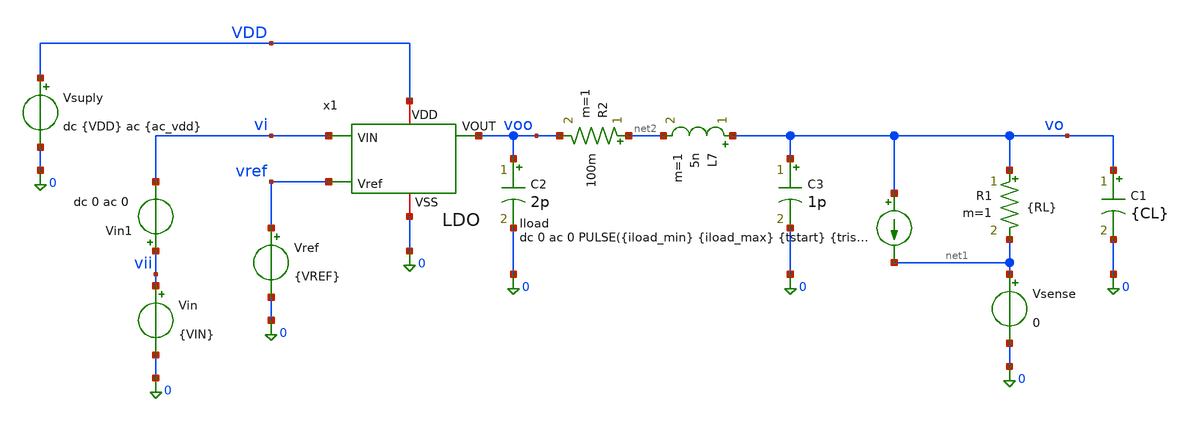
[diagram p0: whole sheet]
** sch_path: xschem/LDO_Top/ldo_tb_pex_montecarlo.sch
**.subckt ldo_tb_pex_montecarlo
Vsuply VDD 0 dc {VDD} ac {ac_vdd}
Vref vref 0 {VREF}
Vin vii 0 {VIN}
R1 vo net1 {RL} m=1
C1 vo 0 {CL} m=1
Iload vo net1 dc 0 ac 0 PULSE({iload_min} {iload_max} {tstart} {trise} {tfall} {twidth} {tperiod})
Vsense net1 0 0
Vin1 vii vi dc 0 ac 0
x1 vi voo VDD vref 0 LDO
C2 voo 0 2p m=1
R2 net2 voo 100m m=1
L7 vo net2 5n m=1
C3 vo 0 1p m=1
**** begin user architecture code


* ==============================================================================
* ENCABEZADO DEL ARCHIVO:
* Script de simulación Monte Carlo Post-Layout (PEX) para el regulador LDO
* completo (incluyendo LDO_pex.spice).
* Evalúa Transitorio (Overshoot/Undershoot), PSRR, Line Regulation,
* Load Regulation y Dropout en cada iteración y guarda en 'datos_mc.txt'
* con el formato exacto que lee el notebook 'LDO_tb_montecarlo.ipynb'.
* ==============================================================================

* 1. Librería de modelos Sky130 con Mismatch (tt_mm) y netlist PEX del LDO
.lib /foss/pdks/sky130A/libs.tech/ngspice/sky130.lib.spice tt_mm
.include /foss/designs/LDO-sky130/xschem/LDO_Top/LDO_pex.spice

.option temp=27
.option num_threads=8
.option gmin=1e-12 reltol=1e-3 abstol=1e-12 vntol=1e-6 itl1=500 itl2=200 itl4=100

.param rsh_var = agauss(0, 0.005, 1)

* Guardar únicamente los nodos clave para no desbordar la RAM con la red RC parásita
.save v(vo) v(voo) v(vi) v(vii) v(vdd) v(vref) v(x1.OTA_0.VO_ota) v(x1.OTA_0.VIP_ota) v(x1.self_bias_0.VR)

* Condiciones iniciales en los nodos reales de LDO_pex.spice para convergencia DC
.nodeset V(vo)=1.2
.nodeset V(voo)=1.2
.nodeset V(x1.OTA_0.VIP_ota)=0.6
.nodeset V(x1.OTA_0.VO_ota)=1.1
.nodeset V(x1.self_bias_0.VR)=0.6
.nodeset V(x1.self_bias_0.vgp_self)=1.0

* Parámetros del LDO
.param VDD = 1.8
.param VREF = 0.6
.param VIN = '1*VDD-0.3'
.param RL = 240e9
.param CL = 1u

* Parámetros para la prueba transitoria de carga
.param iload_min = 1u
.param iload_max = 5m
.param tstart   = 30u
.param trise    = 100n
.param tfall    = 100n
.param twidth   = 100u
.param tperiod  = 200u
.param tsim     = '3*tperiod'

.param ac_iprobe = 0
.param ac_vdd    = 0

* --- Clamp SOLO de simulación (evita soluciones DC falsas en los nodos reales del PEX) ---
Dclpn 0 vo dclamp_tb
Dclpp vo vclp dclamp_tb
Dclpn2 0 x1.OTA_0.VIP_ota dclamp_tb
Dclpp2 x1.OTA_0.VIP_ota vclp dclamp_tb
Vclp vclp 0 5
.model dclamp_tb D(IS=1e-15 N=1)

.control
* =========================================================
* CONFIGURACION DEL BUCLE MONTE CARLO PEX
* =========================================================
let mc_runs = 100
let run = 1

set appendwrite
set filetype=ascii

let tperiod = 200u
let tsim = '3*tperiod'

echo === INICIO MONTE CARLO PEX === > datos_mc.txt

* =========================================================
* INICIO DEL BUCLE
* =========================================================
while run <= mc_runs

    echo ======================================
    echo CORRIENDO MONTE CARLO PEX ITERACION: $&run
    echo ======================================
    echo --- ITERACION: $&run --- >> datos_mc.txt

    * 1. Tirar los dados estadísticos UNA VEZ para esta muestra (chip)
    reset
    set mc_strict = 1

    * -----------------------------------------------------
    * A. TRANSIENTE (Overshoot y Undershoot)
    * -----------------------------------------------------
    alterparam ac_iprobe = 0
    alterparam ac_vdd = 0
    alterparam RL = 240e9
    reset
    save v(vo) v(vi) v(vdd)

    tran 2u $&tsim

    let t_ignorar = 150u
    meas tran v_estable_ligera FIND v(vo) AT=270u
    meas tran v_estable_pesada FIND v(vo) AT=180u
    meas tran vo_max MAX v(vo) from=$&t_ignorar to=$&tsim
    meas tran vo_min MIN v(vo) from=$&t_ignorar to=$&tsim
    meas tran salida_tran avg v(vo) from=$&t_ignorar to=$&tsim

    let undershoot_mV = (v_estable_ligera - vo_min) * 1e3
    let overshoot_mV  = (vo_max - v_estable_pesada) * 1e3

    echo 'undershoot_mV = $&undershoot_mV' >> datos_mc.txt
    echo 'overshoot_mV = $&overshoot_mV' >> datos_mc.txt
    echo 'salida_tran = $&salida_tran' >> datos_mc.txt

    * -----------------------------------------------------
    * B. AC (PSRR)
    * -----------------------------------------------------
    alterparam ac_iprobe = 0
    alterparam ac_vdd = 1
    alterparam RL = 240e9
    reset
    save v(vdd) v(vo)
    alter @Iload[dc] = 5m

    ac dec 10 10 1G
    let psrr1 = v(vdd)/v(vo)
    let psrr_db = vdb(psrr1)

    meas ac gananciaPSRR_1   find psrr_db at=10
    meas ac gananciaPSRR_1k  find psrr_db at=1k
    meas ac gananciaPSRR_10k find psrr_db at=10k
    meas ac gananciaPSRR_1M  find psrr_db at=1Meg

    echo 'psrr_1 = $&gananciaPSRR_1' >> datos_mc.txt
    echo 'psrr_1k = $&gananciaPSRR_1k' >> datos_mc.txt
    echo 'psrr_10k = $&gananciaPSRR_10k' >> datos_mc.txt
    echo 'psrr_1M = $&gananciaPSRR_1M' >> datos_mc.txt

    * -----------------------------------------------------
    * C. TRANSIENTE (Line Regulation)
    * -----------------------------------------------------
    alterparam ac_iprobe = 0
    alterparam ac_vdd = 0
    alterparam RL = 240e9
    reset
    save v(vo) v(vi)

    alter @Vin[pwl] = [ 0 1.4 1m 1.8 ]
    alter @Iload[pwl] = [ 0 1u 1m 1u ]

    tran 2u 1m

    let t_line_ini = 40u
    let t_line_fin = 950u

    meas tran voline_max MAX v(vo) from=$&t_line_ini to=$&t_line_fin
    meas tran voline_min MIN v(vo) from=$&t_line_ini to=$&t_line_fin
    meas tran salida_line avg v(vo) from=$&t_line_ini to=$&t_line_fin
    let line_regulation_mV = (voline_max - voline_min) * 1000

    echo 'line_regulation_mv = $&line_regulation_mV' >> datos_mc.txt
    echo 'salida_line = $&salida_line' >> datos_mc.txt

    * -----------------------------------------------------
    * D. TRANSIENTE (Load Regulation)
    * -----------------------------------------------------
    alterparam RL = 240e9
    reset
    save v(vo)

    alter @Iload[pwl] = [ 0 1u 1m 5m ]

    tran 2u 1m

    meas tran vout_light FIND v(vo) AT=40u
    meas tran vout_heavy FIND v(vo) AT=1m

    let load_regulation_mV = (vout_light - vout_heavy) * 1000

    echo 'load_regulation_mV = $&load_regulation_mV' >> datos_mc.txt

    * -----------------------------------------------------
    * E. TRANSIENTE (Dropout)
    * -----------------------------------------------------
    alterparam RL = 240
    reset
    save v(vo) v(vi)

    alter @Vin[pwl] = [ 0 2 1m 0 ]
    alter @Iload[pwl] = [ 0 1u 1m 1u ]



    meas tran vout_nom FIND v(vo) AT=225u
    let vout_target = vout_nom * 0.90

    meas tran vin_do FIND v(vi) WHEN v(vo) = vout_target fall=1
    let dropout_mV = (vin_do - vout_target) * 1e3

    echo 'dropout_mV = $&dropout_mV' >> datos_mc.txt

    * -----------------------------------------------------
    * Desbloquear la semilla y liberar memoria RAM para la siguiente iteración
    * -----------------------------------------------------
    unset mc_strict
    plot tran2.vo
    destroy tran1 ac1 tran2 tran3 tran4

    let run = run + 1

end

echo === FIN MONTE CARLO PEX === >> datos_mc.txt
echo ======================================
echo SIMULACION MONTE CARLO PEX FINALIZADA
echo ======================================
.endc


**** end user architecture code
**.ends
.end
